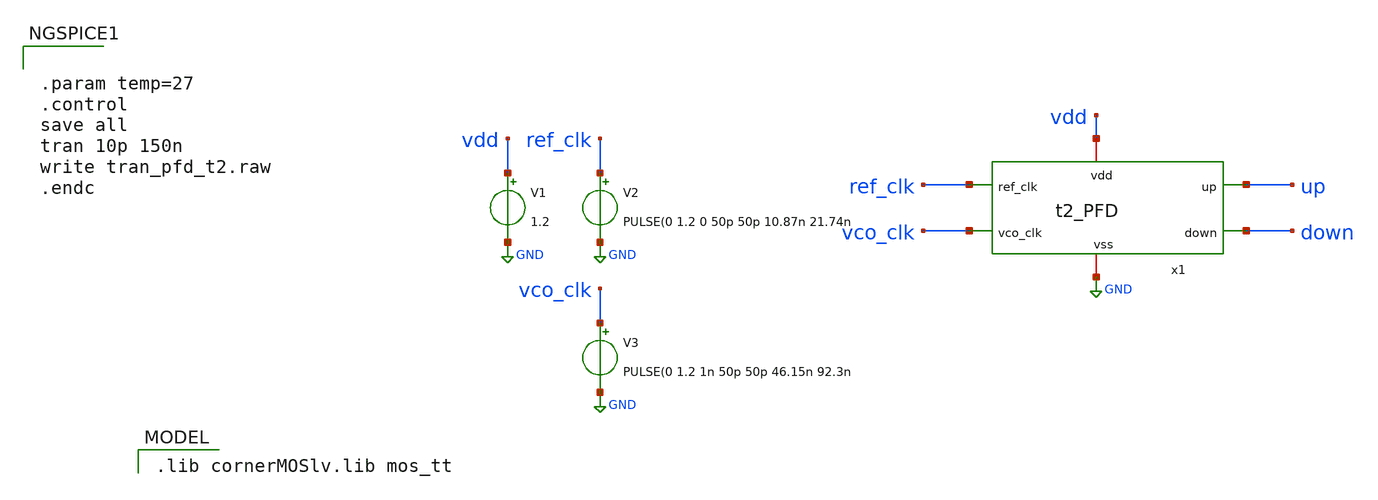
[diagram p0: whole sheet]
** sch_path: Team 2 Design/design_data/xschem/t2_PFD_tb.sch
**.subckt t2_PFD_tb
x1 vdd up GND down ref_clk vco_clk t2_PFD
V1 vdd GND 1.2
V2 ref_clk GND PULSE(0 1.2 0 50p 50p 10.87n 21.74n
V3 vco_clk GND PULSE(0 1.2 1n 50p 50p 46.15n 92.3n
**** begin user architecture code
 .lib cornerMOSlv.lib mos_tt



.param temp=27
.control
save all
tran 10p 150n
write tran_pfd_t2.raw
.endc


**** end user architecture code
**.ends

* expanding   symbol:  t2_PFD.sym # of pins=6
** sym_path: Team 2 Design/design_data/xschem/t2_PFD.sym
** sch_path: Team 2 Design/design_data/xschem/t2_PFD.sch
.subckt t2_PFD vdd up vss down ref_clk vco_clk
*.iopin vdd
*.ipin ref_clk
*.iopin vss
*.ipin vco_clk
*.opin up
*.opin down
XM1 net2 vco_clk vss vss sg13_lv_nmos w=0.36u l=0.15u ng=1 m=1 mm_ok=1
XM4 net1 ref_clk net2 vss sg13_lv_nmos w=1.8u l=0.15u ng=1 m=1 mm_ok=1
XM5 net3 ref_clk net1 vss sg13_lv_nmos w=0.84u l=0.15u ng=1 m=1 mm_ok=1
XM9 net3 ref_clk ref_clk vdd sg13_lv_pmos w=0.64u l=0.15u ng=1 m=1 mm_ok=1
XM11 net7 net3 vss vss sg13_lv_nmos w=0.36u l=0.15u ng=1 m=1 mm_ok=1
XM12 vdd net3 net7 vdd sg13_lv_pmos w=0.72u l=0.15u ng=1 m=1 mm_ok=1
XM13 up net7 vss vss sg13_lv_nmos w=0.48u l=0.15u ng=1 m=1 mm_ok=1
XM14 vdd net7 up vdd sg13_lv_pmos w=0.96u l=0.15u ng=1 m=1 mm_ok=1
XM3 net1 ref_clk vdd vdd sg13_lv_pmos w=0.64u l=0.15u ng=1 m=1 mm_ok=1
XM6 net4 vco_clk vdd vdd sg13_lv_pmos w=0.64u l=0.15u ng=1 m=1 mm_ok=1
XM7 net4 vco_clk net5 vss sg13_lv_nmos w=1.8u l=0.15u ng=1 m=1 mm_ok=1
XM19 net5 ref_clk vss vss sg13_lv_nmos w=0.36u l=0.15u ng=1 m=1 mm_ok=1
XM8 net6 vco_clk net4 vss sg13_lv_nmos w=0.84u l=0.15u ng=1 m=1 mm_ok=1
XM10 net6 vco_clk vco_clk vdd sg13_lv_pmos w=0.64u l=0.15u ng=1 m=1 mm_ok=1
XM15 vdd net6 net8 vdd sg13_lv_pmos w=0.72u l=0.15u ng=1 m=1 mm_ok=1
XM16 net8 net6 vss vss sg13_lv_nmos w=0.36u l=0.15u ng=1 m=1 mm_ok=1
XM17 vdd net8 down vdd sg13_lv_pmos w=0.96u l=0.15u ng=1 m=1 mm_ok=1
XM18 down net8 vss vss sg13_lv_nmos w=0.48u l=0.15u ng=1 m=1 mm_ok=1
.ends

.GLOBAL GND
.end
